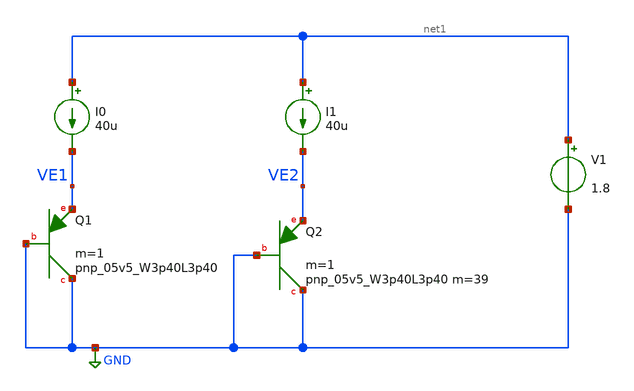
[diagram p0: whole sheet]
** sch_path: design/bgr_new/PTAT.sch
**.subckt PTAT
XQ1 GND GND VE1 sky130_fd_pr__pnp_05v5_W3p40L3p40 m=1
I0 net1 VE1 40u
V1 net1 GND 1.8
I1 net1 VE2 40u
XQ2 GND GND VE2 sky130_fd_pr__pnp_05v5_W3p40L3p40 m=39 m=1
**** begin user architecture code

** opencircuitdesign pdks install
.lib $::SKYWATER_MODELS/sky130.lib.spice tt




.options savecurrents


*** plot vbgp with variation in supply voltage
*Vdd VDD GND 3.3
*V_en en GND 3.3
*.dc Vdd 2 4 0.1
*.control
*run
*print Vbgp
*plot V(Vbgp)
*.endc

*** plot vbgp with variation in temperature @3.3V
*Vdd VDD GND 3.3
*V_en en GND 3.3
.dc temp -20 100 0.1
.control
save all
run
print V(VE1) V(VE2)
plot V(VE1) V(VE2)
plot deriv(V(VE1)) deriv(V(VE2))
let delta = V(VE1)-V(VE2)
plot delta
plot deriv(delta)
let is1=@q.xq1.qsky130_fd_pr__pnp_05v5_w3p40l3p40[is]
plot is1
.endc

*** plot voltage coefficient
*Vdd VDD GND 3.3
*V_en en GND 3.3
*.dc Vdd 2 4 0.1
*.control
*run
*plot deriv(V(Vbgp))
*.endc

*** plot temperature coefficient
*Vdd VDD GND 3.3
*V_en en GND 3.3
*.dc temp -40 140 1
*.control
*run
*plot deriv(V(Vbgp))/1.202344
*.endc



*** enable pin
*Vdd VDD GND 3.3
*V_en en GND PULSE(0 3.3 0 200us 200us 600us 2000us 0)
*.tran 1u 2000us
*.control
*run
*plot V(en)
*plot -I(VDD)
*.endc


**** end user architecture code
**.ends
.GLOBAL GND
.end
